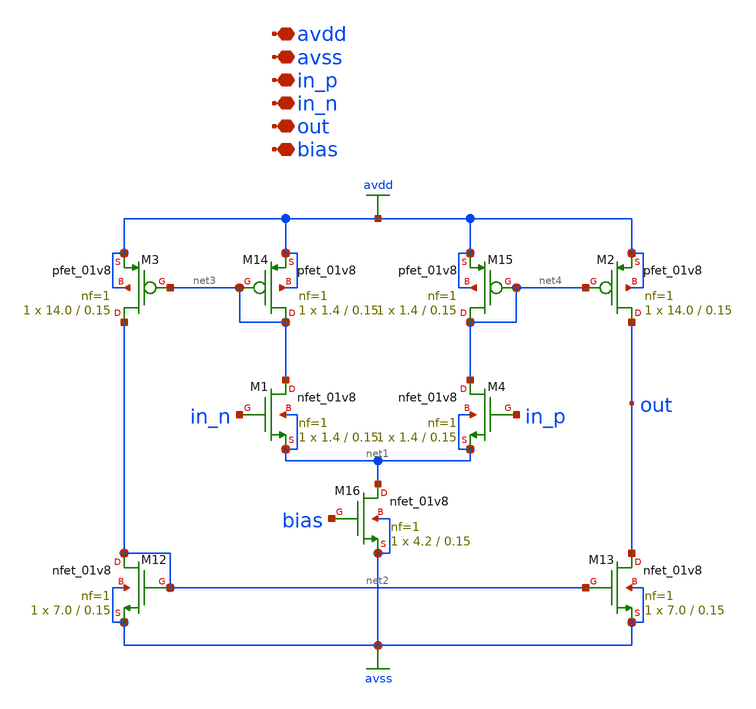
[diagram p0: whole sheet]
** sch_path: xschem/ota_2.sch
**.subckt ota_2 avdd avss in_p in_n out bias
*.iopin avdd
*.iopin avss
*.iopin in_p
*.iopin in_n
*.iopin out
*.iopin bias
XM1 net3 in_n net1 net1 sky130_fd_pr__nfet_01v8 L=0.15 W=1.4 nf=1 ad='int((nf+1)/2) * W/nf * 0.29' as='int((nf+2)/2) * W/nf * 0.29'
+ pd='2*int((nf+1)/2) * (W/nf + 0.29)' ps='2*int((nf+2)/2) * (W/nf + 0.29)' nrd='0.29 / W' nrs='0.29 / W'
+ sa=0 sb=0 sd=0 mult=1 m=1
XM3 net2 net3 avdd avdd sky130_fd_pr__pfet_01v8 L=0.15 W=14.0 nf=1 ad='int((nf+1)/2) * W/nf * 0.29' as='int((nf+2)/2) * W/nf * 0.29'
+ pd='2*int((nf+1)/2) * (W/nf + 0.29)' ps='2*int((nf+2)/2) * (W/nf + 0.29)' nrd='0.29 / W' nrs='0.29 / W'
+ sa=0 sb=0 sd=0 mult=1 m=1
XM2 out net4 avdd avdd sky130_fd_pr__pfet_01v8 L=0.15 W=14.0 nf=1 ad='int((nf+1)/2) * W/nf * 0.29' as='int((nf+2)/2) * W/nf * 0.29'
+ pd='2*int((nf+1)/2) * (W/nf + 0.29)' ps='2*int((nf+2)/2) * (W/nf + 0.29)' nrd='0.29 / W' nrs='0.29 / W'
+ sa=0 sb=0 sd=0 mult=1 m=1
XM4 net4 in_p net1 net1 sky130_fd_pr__nfet_01v8 L=0.15 W=1.4 nf=1 ad='int((nf+1)/2) * W/nf * 0.29' as='int((nf+2)/2) * W/nf * 0.29'
+ pd='2*int((nf+1)/2) * (W/nf + 0.29)' ps='2*int((nf+2)/2) * (W/nf + 0.29)' nrd='0.29 / W' nrs='0.29 / W'
+ sa=0 sb=0 sd=0 mult=1 m=1
XM12 net2 net2 avss avss sky130_fd_pr__nfet_01v8 L=0.15 W=7.0 nf=1 ad='int((nf+1)/2) * W/nf * 0.29' as='int((nf+2)/2) * W/nf * 0.29'
+ pd='2*int((nf+1)/2) * (W/nf + 0.29)' ps='2*int((nf+2)/2) * (W/nf + 0.29)' nrd='0.29 / W' nrs='0.29 / W'
+ sa=0 sb=0 sd=0 mult=1 m=1
XM13 out net2 avss avss sky130_fd_pr__nfet_01v8 L=0.15 W=7.0 nf=1 ad='int((nf+1)/2) * W/nf * 0.29' as='int((nf+2)/2) * W/nf * 0.29'
+ pd='2*int((nf+1)/2) * (W/nf + 0.29)' ps='2*int((nf+2)/2) * (W/nf + 0.29)' nrd='0.29 / W' nrs='0.29 / W'
+ sa=0 sb=0 sd=0 mult=1 m=1
XM14 net3 net3 avdd avdd sky130_fd_pr__pfet_01v8 L=0.15 W=1.4 nf=1 ad='int((nf+1)/2) * W/nf * 0.29' as='int((nf+2)/2) * W/nf * 0.29'
+ pd='2*int((nf+1)/2) * (W/nf + 0.29)' ps='2*int((nf+2)/2) * (W/nf + 0.29)' nrd='0.29 / W' nrs='0.29 / W'
+ sa=0 sb=0 sd=0 mult=1 m=1
XM15 net4 net4 avdd avdd sky130_fd_pr__pfet_01v8 L=0.15 W=1.4 nf=1 ad='int((nf+1)/2) * W/nf * 0.29' as='int((nf+2)/2) * W/nf * 0.29'
+ pd='2*int((nf+1)/2) * (W/nf + 0.29)' ps='2*int((nf+2)/2) * (W/nf + 0.29)' nrd='0.29 / W' nrs='0.29 / W'
+ sa=0 sb=0 sd=0 mult=1 m=1
XM16 net1 bias avss avss sky130_fd_pr__nfet_01v8 L=0.15 W=4.2 nf=1 ad='int((nf+1)/2) * W/nf * 0.29' as='int((nf+2)/2) * W/nf * 0.29'
+ pd='2*int((nf+1)/2) * (W/nf + 0.29)' ps='2*int((nf+2)/2) * (W/nf + 0.29)' nrd='0.29 / W' nrs='0.29 / W'
+ sa=0 sb=0 sd=0 mult=1 m=1
**.ends
.GLOBAL avdd
.GLOBAL avss
.end
